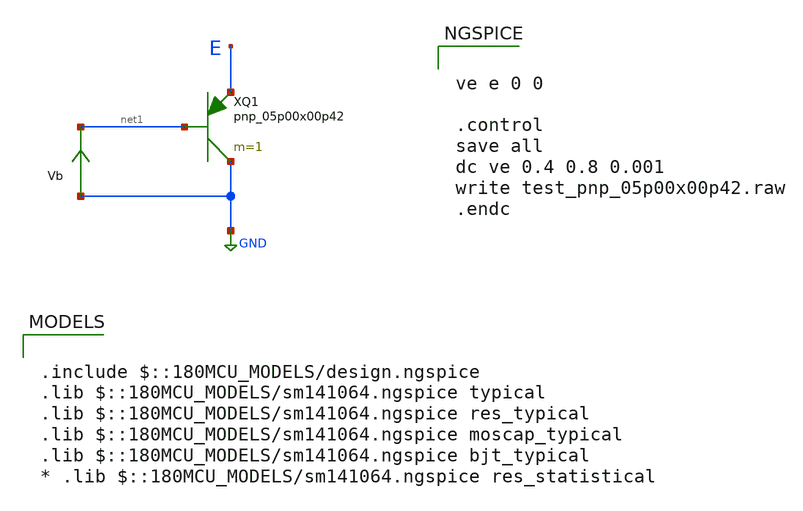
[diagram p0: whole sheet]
** sch_path: gf180mcuD/xschem_libs/gf180mcu_tests/test_pnp_05p00x00p42/schematic/test_pnp_05p00x00p42.sch
* Copyright 2022 GlobalFoundries PDK Authors
* Licensed under the Apache License, Version 2.0 (the "License");
* you may not use this file except in compliance with the License.
* You may obtain a copy of the License at
* https://www.apache.org/licenses/LICENSE-2.0
* Unless required by applicable law or agreed to in writing, software
* distributed under the License is distributed on an "AS IS" BASIS,
* WITHOUT WARRANTIES OR CONDITIONS OF ANY KIND, either express or implied.
* See the License for the specific language governing permissions and
* limitations under the License.
**.subckt test_pnp_05p00x00p42
XQ1 GND net1 E pnp_05p00x00p42 m=1
Vb GND net1 0
.save i(vb)
**** begin user architecture code

.include $::180MCU_MODELS/design.ngspice
.lib $::180MCU_MODELS/sm141064.ngspice typical
.lib $::180MCU_MODELS/sm141064.ngspice res_typical
.lib $::180MCU_MODELS/sm141064.ngspice moscap_typical
.lib $::180MCU_MODELS/sm141064.ngspice bjt_typical
* .lib $::180MCU_MODELS/sm141064.ngspice res_statistical



ve e 0 0

.control
save all
dc ve 0.4 0.8 0.001
write test_pnp_05p00x00p42.raw
.endc


**** end user architecture code
**.ends
.GLOBAL GND
.end
